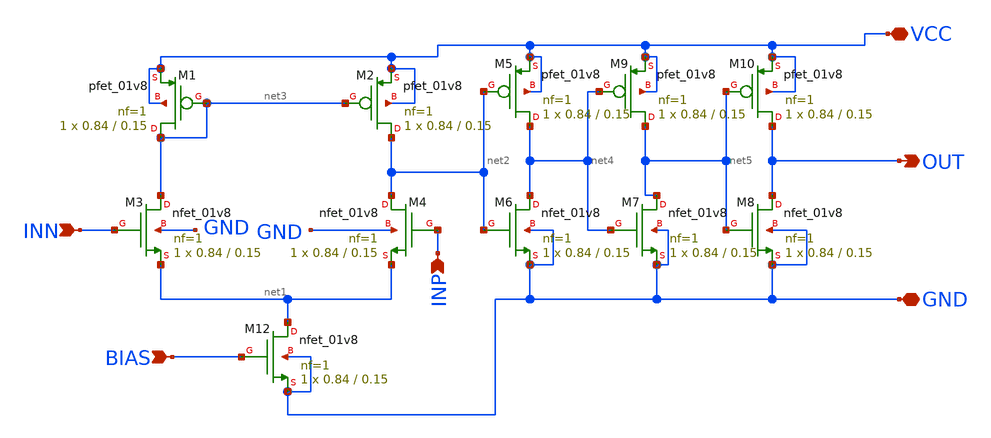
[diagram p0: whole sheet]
** sch_path: week7/pre-layout/comp.sch
**.subckt comp BIAS VCC GND OUT INN INP
*.ipin BIAS
*.iopin VCC
*.iopin GND
*.opin OUT
*.ipin INN
*.ipin INP
XM1 net3 net3 VCC VCC sky130_fd_pr__pfet_01v8 L=0.15 W=0.84 nf=1 ad='int((nf+1)/2) * W/nf * 0.29' as='int((nf+2)/2) * W/nf * 0.29'
+ pd='2*int((nf+1)/2) * (W/nf + 0.29)' ps='2*int((nf+2)/2) * (W/nf + 0.29)' nrd='0.29 / W' nrs='0.29 / W'
+ sa=0 sb=0 sd=0 mult=1 m=1
XM3 net3 INN net1 GND sky130_fd_pr__nfet_01v8 L=0.15 W=0.84 nf=1 ad='int((nf+1)/2) * W/nf * 0.29' as='int((nf+2)/2) * W/nf * 0.29'
+ pd='2*int((nf+1)/2) * (W/nf + 0.29)' ps='2*int((nf+2)/2) * (W/nf + 0.29)' nrd='0.29 / W' nrs='0.29 / W'
+ sa=0 sb=0 sd=0 mult=1 m=1
XM12 net1 BIAS GND GND sky130_fd_pr__nfet_01v8 L=0.15 W=0.84 nf=1 ad='int((nf+1)/2) * W/nf * 0.29' as='int((nf+2)/2) * W/nf * 0.29'
+ pd='2*int((nf+1)/2) * (W/nf + 0.29)' ps='2*int((nf+2)/2) * (W/nf + 0.29)' nrd='0.29 / W' nrs='0.29 / W'
+ sa=0 sb=0 sd=0 mult=1 m=1
XM2 net2 net3 VCC VCC sky130_fd_pr__pfet_01v8 L=0.15 W=0.84 nf=1 ad='int((nf+1)/2) * W/nf * 0.29' as='int((nf+2)/2) * W/nf * 0.29'
+ pd='2*int((nf+1)/2) * (W/nf + 0.29)' ps='2*int((nf+2)/2) * (W/nf + 0.29)' nrd='0.29 / W' nrs='0.29 / W'
+ sa=0 sb=0 sd=0 mult=1 m=1
XM4 net2 INP net1 GND sky130_fd_pr__nfet_01v8 L=0.15 W=0.84 nf=1 ad='int((nf+1)/2) * W/nf * 0.29' as='int((nf+2)/2) * W/nf * 0.29'
+ pd='2*int((nf+1)/2) * (W/nf + 0.29)' ps='2*int((nf+2)/2) * (W/nf + 0.29)' nrd='0.29 / W' nrs='0.29 / W'
+ sa=0 sb=0 sd=0 mult=1 m=1
XM5 net4 net2 VCC VCC sky130_fd_pr__pfet_01v8 L=0.15 W=0.84 nf=1 ad='int((nf+1)/2) * W/nf * 0.29' as='int((nf+2)/2) * W/nf * 0.29'
+ pd='2*int((nf+1)/2) * (W/nf + 0.29)' ps='2*int((nf+2)/2) * (W/nf + 0.29)' nrd='0.29 / W' nrs='0.29 / W'
+ sa=0 sb=0 sd=0 mult=1 m=1
XM6 net4 net2 GND GND sky130_fd_pr__nfet_01v8 L=0.15 W=0.84 nf=1 ad='int((nf+1)/2) * W/nf * 0.29' as='int((nf+2)/2) * W/nf * 0.29'
+ pd='2*int((nf+1)/2) * (W/nf + 0.29)' ps='2*int((nf+2)/2) * (W/nf + 0.29)' nrd='0.29 / W' nrs='0.29 / W'
+ sa=0 sb=0 sd=0 mult=1 m=1
XM7 net5 net4 GND GND sky130_fd_pr__nfet_01v8 L=0.15 W=0.84 nf=1 ad='int((nf+1)/2) * W/nf * 0.29' as='int((nf+2)/2) * W/nf * 0.29'
+ pd='2*int((nf+1)/2) * (W/nf + 0.29)' ps='2*int((nf+2)/2) * (W/nf + 0.29)' nrd='0.29 / W' nrs='0.29 / W'
+ sa=0 sb=0 sd=0 mult=1 m=1
XM8 OUT net5 GND GND sky130_fd_pr__nfet_01v8 L=0.15 W=0.84 nf=1 ad='int((nf+1)/2) * W/nf * 0.29' as='int((nf+2)/2) * W/nf * 0.29'
+ pd='2*int((nf+1)/2) * (W/nf + 0.29)' ps='2*int((nf+2)/2) * (W/nf + 0.29)' nrd='0.29 / W' nrs='0.29 / W'
+ sa=0 sb=0 sd=0 mult=1 m=1
XM9 net5 net4 VCC VCC sky130_fd_pr__pfet_01v8 L=0.15 W=0.84 nf=1 ad='int((nf+1)/2) * W/nf * 0.29' as='int((nf+2)/2) * W/nf * 0.29'
+ pd='2*int((nf+1)/2) * (W/nf + 0.29)' ps='2*int((nf+2)/2) * (W/nf + 0.29)' nrd='0.29 / W' nrs='0.29 / W'
+ sa=0 sb=0 sd=0 mult=1 m=1
XM10 OUT net5 VCC VCC sky130_fd_pr__pfet_01v8 L=0.15 W=0.84 nf=1 ad='int((nf+1)/2) * W/nf * 0.29' as='int((nf+2)/2) * W/nf * 0.29'
+ pd='2*int((nf+1)/2) * (W/nf + 0.29)' ps='2*int((nf+2)/2) * (W/nf + 0.29)' nrd='0.29 / W' nrs='0.29 / W'
+ sa=0 sb=0 sd=0 mult=1 m=1
**.ends
.end
